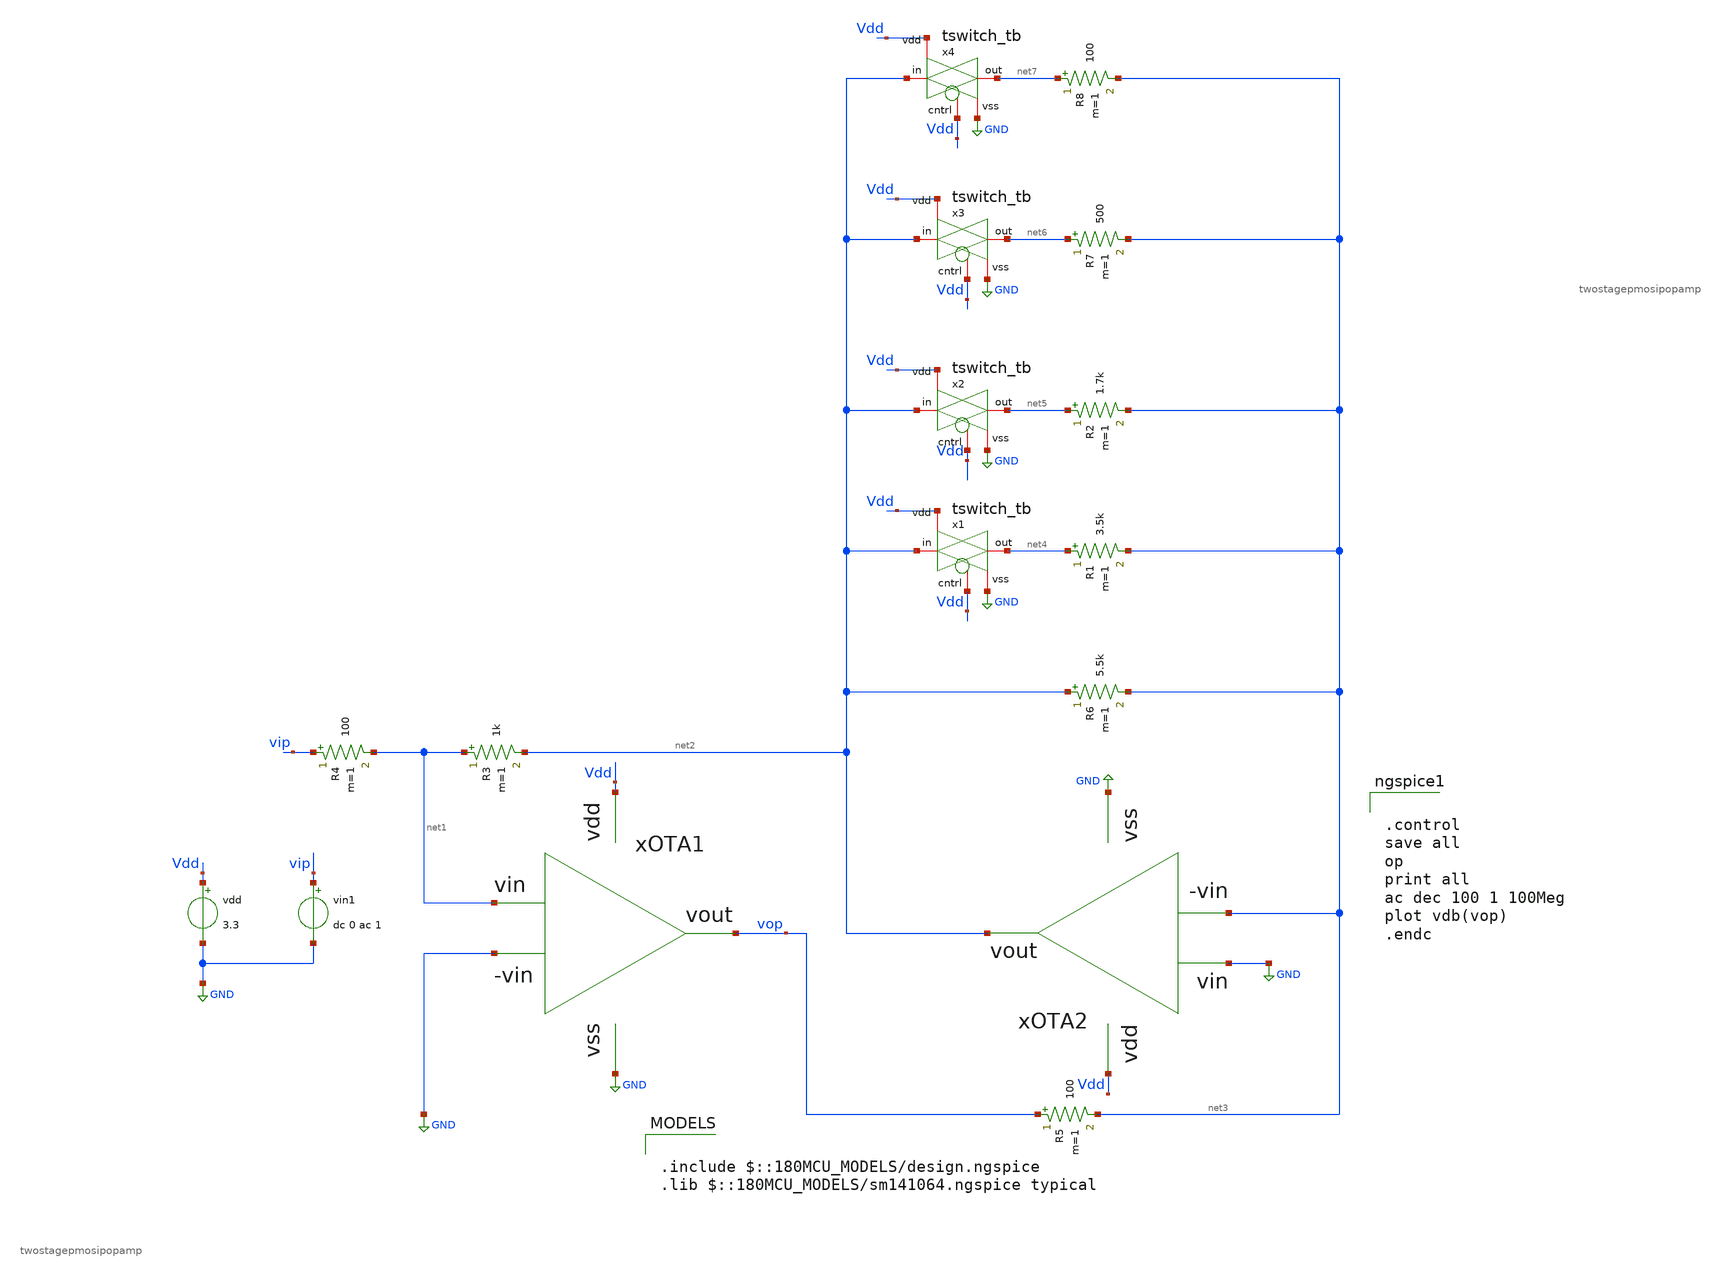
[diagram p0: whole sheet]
** sch_path: designs/pga2.sch
**.subckt pga2
xOTA1 net1 Vdd GND vop GND twostagepmosipopamp
xOTA2 GND Vdd net3 net2 GND twostagepmosipopamp
R3 net1 net2 1k m=1
R4 vip net1 100 m=1
R5 vop net3 100 m=1
R6 net2 net3 5.5k m=1
vdd Vdd GND 3.3
vin1 vip GND dc 0 ac 1
x1 Vdd net2 net4 Vdd GND tswitch_tb
R1 net4 net3 3.5k m=1
x2 Vdd net2 net5 Vdd GND tswitch_tb
R2 net5 net3 1.7k m=1
x3 Vdd net2 net6 Vdd GND tswitch_tb
R7 net6 net3 500 m=1
R8 net7 net3 100 m=1
x4 Vdd net2 net7 Vdd GND tswitch_tb
**** begin user architecture code

.include $::180MCU_MODELS/design.ngspice
.lib $::180MCU_MODELS/sm141064.ngspice typical



.control
save all
op
print all
ac dec 100 1 100Meg
plot vdb(vop)
.endc

**** end user architecture code
**.ends
.GLOBAL GND
.end
